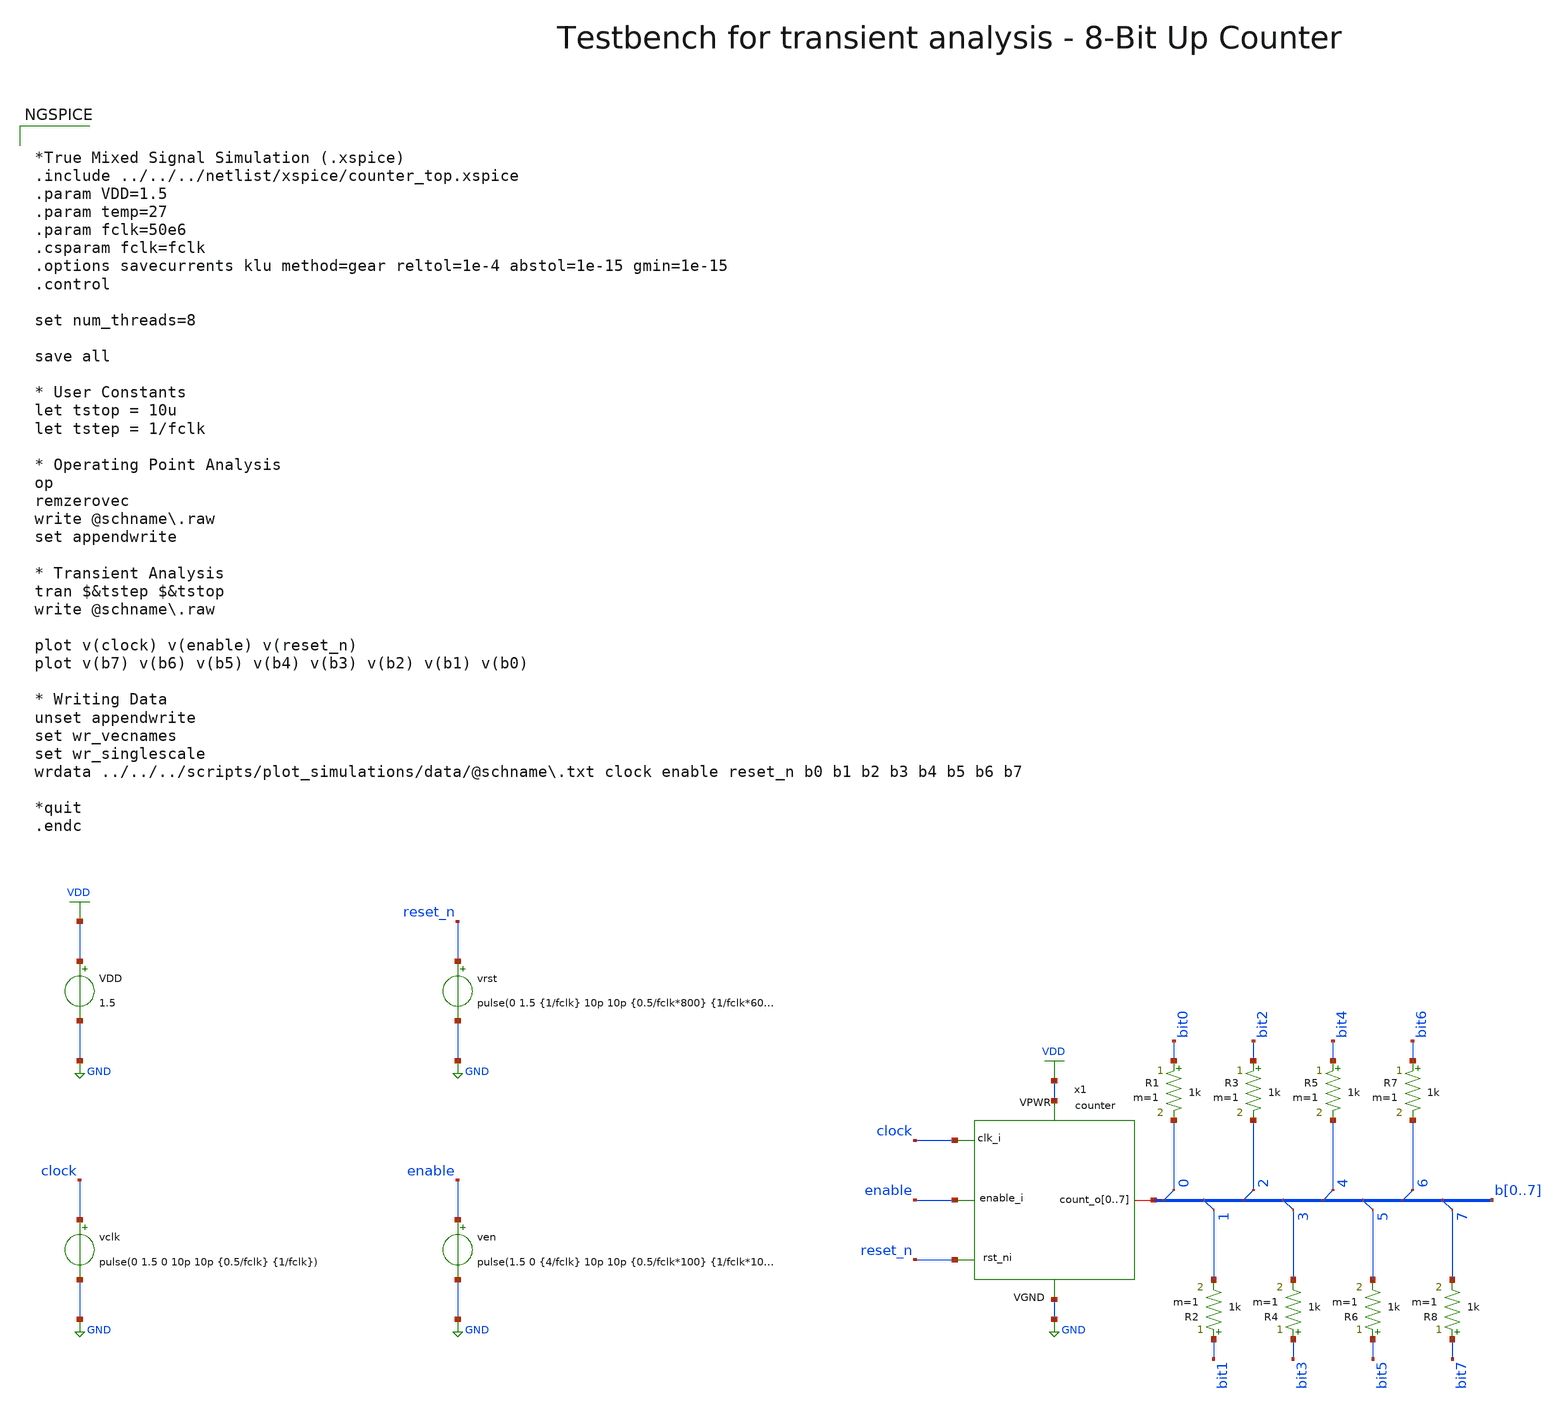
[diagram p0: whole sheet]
** sch_path: macros/heichips26_digital_project/macros/counter/testbenches/xschem/counter_tb_tran.sch
**.subckt counter_tb_tran
VDD VDD GND 1.5
vclk clock GND pulse(0 1.5 0 10p 10p {0.5/fclk} {1/fclk})
vrst reset_n GND pulse(0 1.5 {1/fclk} 10p 10p {0.5/fclk*800} {1/fclk*600} 1)
ven enable GND pulse(1.5 0 {4/fclk} 10p 10p {0.5/fclk*100} {1/fclk*100} 1)
x1 VDD GND clock reset_n enable b0 b1 b2 b3 b4 b5 b6 b7 counter
* tap: b[0..7] --> b0
R1 bit0 b0 1k m=1
* tap: b[0..7] --> b1
R2 bit1 b1 1k m=1
* tap: b[0..7] --> b2
R3 bit2 b2 1k m=1
* tap: b[0..7] --> b3
R4 bit3 b3 1k m=1
* tap: b[0..7] --> b4
R5 bit4 b4 1k m=1
* tap: b[0..7] --> b5
R6 bit5 b5 1k m=1
* tap: b[0..7] --> b6
R7 bit6 b6 1k m=1
* tap: b[0..7] --> b7
R8 bit7 b7 1k m=1
**** begin user architecture code


*True Mixed Signal Simulation (.xspice)
.include ../../../netlist/xspice/counter_top.xspice
.param VDD=1.5
.param temp=27
.param fclk=50e6
.csparam fclk=fclk
.options savecurrents klu method=gear reltol=1e-4 abstol=1e-15 gmin=1e-15
.control

set num_threads=8

save all

* User Constants
let tstop = 10u
let tstep = 1/fclk

* Operating Point Analysis
op
remzerovec
write @schname\.raw
set appendwrite

* Transient Analysis
tran $&tstep $&tstop
write @schname\.raw

plot v(clock) v(enable) v(reset_n)
plot v(b7) v(b6) v(b5) v(b4) v(b3) v(b2) v(b1) v(b0)

* Writing Data
unset appendwrite
set wr_vecnames
set wr_singlescale
wrdata ../../../scripts/plot_simulations/data/@schname\.txt clock enable reset_n b0 b1 b2 b3 b4 b5
+ b6 b7

*quit
.endc


.lib cornerMOSlv.lib mos_tt
.lib cornerMOShv.lib mos_tt
.lib cornerHBT.lib hbt_typ
.lib cornerRES.lib res_typ
.lib cornerCAP.lib cap_typ
.lib cornerDIO.lib dio_tt

**** end user architecture code
**.ends
.GLOBAL GND
.GLOBAL VDD
.end
